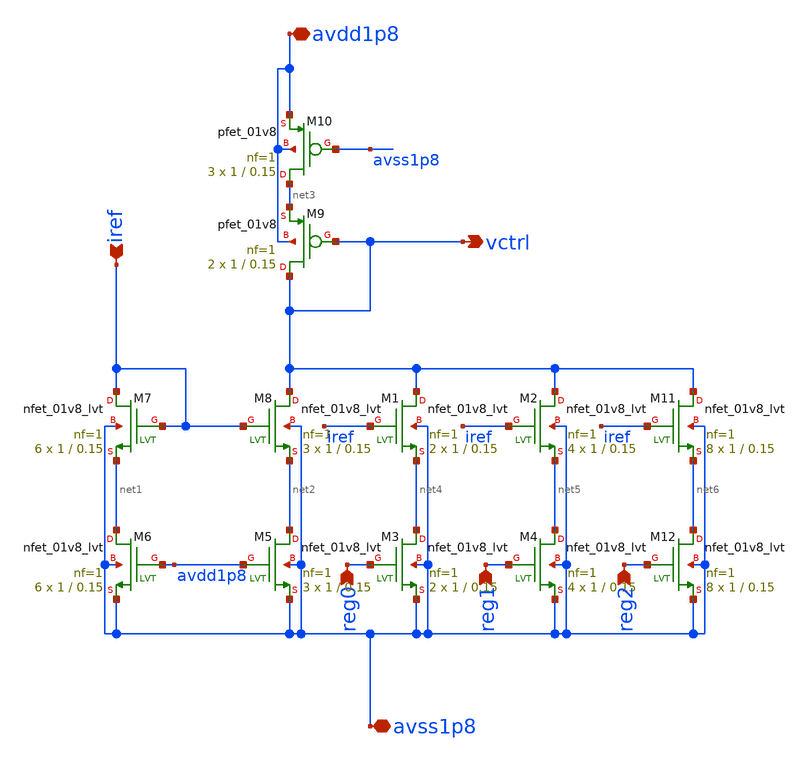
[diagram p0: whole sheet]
** sch_path: xschem/iref_ctrl_res_amp.sch
**.subckt iref_ctrl_res_amp avdd1p8 avss1p8 reg0 reg1 reg2 vctrl iref
*.iopin avdd1p8
*.iopin avss1p8
*.ipin reg0
*.ipin reg1
*.ipin reg2
*.opin vctrl
*.ipin iref
XM7 iref iref net1 avss1p8 sky130_fd_pr__nfet_01v8_lvt L=0.15 W=1 nf=1 ad='int((nf+1)/2) * W/nf * 0.29'
+ as='int((nf+2)/2) * W/nf * 0.29' pd='2*int((nf+1)/2) * (W/nf + 0.29)' ps='2*int((nf+2)/2) * (W/nf + 0.29)'
+ nrd='0.29 / W' nrs='0.29 / W' sa=0 sb=0 sd=0 mult=6 m=6
XM8 vctrl iref net2 avss1p8 sky130_fd_pr__nfet_01v8_lvt L=0.15 W=1 nf=1 ad='int((nf+1)/2) * W/nf * 0.29'
+ as='int((nf+2)/2) * W/nf * 0.29' pd='2*int((nf+1)/2) * (W/nf + 0.29)' ps='2*int((nf+2)/2) * (W/nf + 0.29)'
+ nrd='0.29 / W' nrs='0.29 / W' sa=0 sb=0 sd=0 mult=3 m=3
XM9 vctrl vctrl net3 avdd1p8 sky130_fd_pr__pfet_01v8 L=0.15 W=1 nf=1 ad='int((nf+1)/2) * W/nf * 0.29'
+ as='int((nf+2)/2) * W/nf * 0.29' pd='2*int((nf+1)/2) * (W/nf + 0.29)' ps='2*int((nf+2)/2) * (W/nf + 0.29)'
+ nrd='0.29 / W' nrs='0.29 / W' sa=0 sb=0 sd=0 mult=2 m=2
XM10 net3 avss1p8 avdd1p8 avdd1p8 sky130_fd_pr__pfet_01v8 L=0.15 W=1 nf=1 ad='int((nf+1)/2) * W/nf * 0.29'
+ as='int((nf+2)/2) * W/nf * 0.29' pd='2*int((nf+1)/2) * (W/nf + 0.29)' ps='2*int((nf+2)/2) * (W/nf + 0.29)'
+ nrd='0.29 / W' nrs='0.29 / W' sa=0 sb=0 sd=0 mult=3 m=3
XM1 vctrl iref net4 avss1p8 sky130_fd_pr__nfet_01v8_lvt L=0.15 W=1 nf=1 ad='int((nf+1)/2) * W/nf * 0.29'
+ as='int((nf+2)/2) * W/nf * 0.29' pd='2*int((nf+1)/2) * (W/nf + 0.29)' ps='2*int((nf+2)/2) * (W/nf + 0.29)'
+ nrd='0.29 / W' nrs='0.29 / W' sa=0 sb=0 sd=0 mult=2 m=2
XM2 vctrl iref net5 avss1p8 sky130_fd_pr__nfet_01v8_lvt L=0.15 W=1 nf=1 ad='int((nf+1)/2) * W/nf * 0.29'
+ as='int((nf+2)/2) * W/nf * 0.29' pd='2*int((nf+1)/2) * (W/nf + 0.29)' ps='2*int((nf+2)/2) * (W/nf + 0.29)'
+ nrd='0.29 / W' nrs='0.29 / W' sa=0 sb=0 sd=0 mult=4 m=4
XM3 net4 reg0 avss1p8 avss1p8 sky130_fd_pr__nfet_01v8_lvt L=0.15 W=1 nf=1 ad='int((nf+1)/2) * W/nf * 0.29'
+ as='int((nf+2)/2) * W/nf * 0.29' pd='2*int((nf+1)/2) * (W/nf + 0.29)' ps='2*int((nf+2)/2) * (W/nf + 0.29)'
+ nrd='0.29 / W' nrs='0.29 / W' sa=0 sb=0 sd=0 mult=2 m=2
XM4 net5 reg1 avss1p8 avss1p8 sky130_fd_pr__nfet_01v8_lvt L=0.15 W=1 nf=1 ad='int((nf+1)/2) * W/nf * 0.29'
+ as='int((nf+2)/2) * W/nf * 0.29' pd='2*int((nf+1)/2) * (W/nf + 0.29)' ps='2*int((nf+2)/2) * (W/nf + 0.29)'
+ nrd='0.29 / W' nrs='0.29 / W' sa=0 sb=0 sd=0 mult=4 m=4
XM5 net2 avdd1p8 avss1p8 avss1p8 sky130_fd_pr__nfet_01v8_lvt L=0.15 W=1 nf=1 ad='int((nf+1)/2) * W/nf * 0.29'
+ as='int((nf+2)/2) * W/nf * 0.29' pd='2*int((nf+1)/2) * (W/nf + 0.29)' ps='2*int((nf+2)/2) * (W/nf + 0.29)'
+ nrd='0.29 / W' nrs='0.29 / W' sa=0 sb=0 sd=0 mult=3 m=3
XM6 net1 avdd1p8 avss1p8 avss1p8 sky130_fd_pr__nfet_01v8_lvt L=0.15 W=1 nf=1 ad='int((nf+1)/2) * W/nf * 0.29'
+ as='int((nf+2)/2) * W/nf * 0.29' pd='2*int((nf+1)/2) * (W/nf + 0.29)' ps='2*int((nf+2)/2) * (W/nf + 0.29)'
+ nrd='0.29 / W' nrs='0.29 / W' sa=0 sb=0 sd=0 mult=6 m=6
XM11 vctrl iref net6 avss1p8 sky130_fd_pr__nfet_01v8_lvt L=0.15 W=1 nf=1 ad='int((nf+1)/2) * W/nf * 0.29'
+ as='int((nf+2)/2) * W/nf * 0.29' pd='2*int((nf+1)/2) * (W/nf + 0.29)' ps='2*int((nf+2)/2) * (W/nf + 0.29)'
+ nrd='0.29 / W' nrs='0.29 / W' sa=0 sb=0 sd=0 mult=8 m=8
XM12 net6 reg2 avss1p8 avss1p8 sky130_fd_pr__nfet_01v8_lvt L=0.15 W=1 nf=1 ad='int((nf+1)/2) * W/nf * 0.29'
+ as='int((nf+2)/2) * W/nf * 0.29' pd='2*int((nf+1)/2) * (W/nf + 0.29)' ps='2*int((nf+2)/2) * (W/nf + 0.29)'
+ nrd='0.29 / W' nrs='0.29 / W' sa=0 sb=0 sd=0 mult=8 m=8
**.ends
.end
